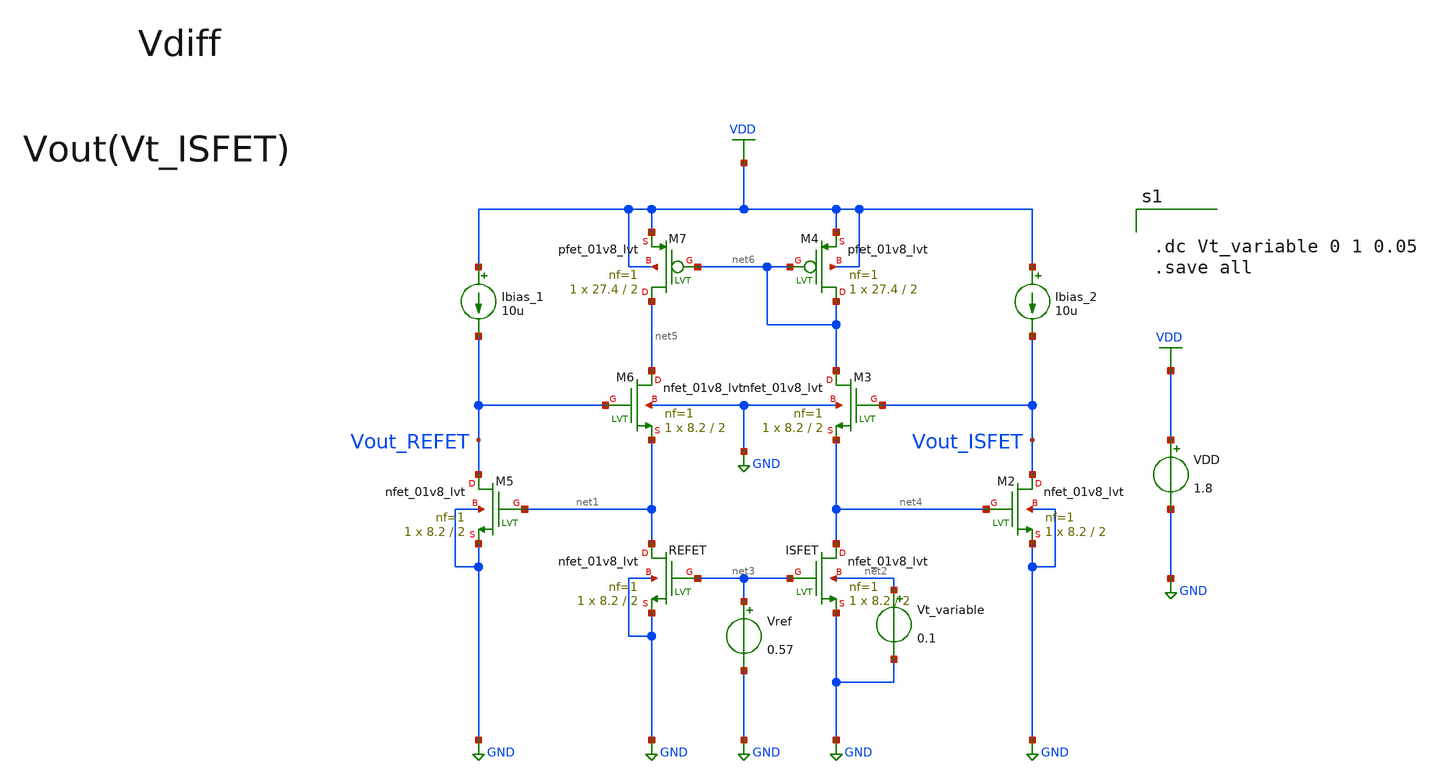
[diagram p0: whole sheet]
** sch_path: Voltage_Clamped_Configuration.sch
**.subckt Voltage_Clamped_Configuration
XISFET net4 net3 GND net2 sky130_fd_pr__nfet_01v8_lvt L=2 W=8.2 nf=1 ad='int((nf+1)/2) * W/nf * 0.29'
+ as='int((nf+2)/2) * W/nf * 0.29' pd='2*int((nf+1)/2) * (W/nf + 0.29)' ps='2*int((nf+2)/2) * (W/nf + 0.29)'
+ nrd='0.29 / W' nrs='0.29 / W' sa=0 sb=0 sd=0 mult=1 m=1
XM4 net6 net6 VDD VDD sky130_fd_pr__pfet_01v8_lvt L=2 W=27.4 nf=1 ad='int((nf+1)/2) * W/nf * 0.29' as='int((nf+2)/2) * W/nf * 0.29'
+ pd='2*int((nf+1)/2) * (W/nf + 0.29)' ps='2*int((nf+2)/2) * (W/nf + 0.29)' nrd='0.29 / W' nrs='0.29 / W'
+ sa=0 sb=0 sd=0 mult=1 m=1
XREFET net1 net3 GND GND sky130_fd_pr__nfet_01v8_lvt L=2 W=8.2 nf=1 ad='int((nf+1)/2) * W/nf * 0.29'
+ as='int((nf+2)/2) * W/nf * 0.29' pd='2*int((nf+1)/2) * (W/nf + 0.29)' ps='2*int((nf+2)/2) * (W/nf + 0.29)'
+ nrd='0.29 / W' nrs='0.29 / W' sa=0 sb=0 sd=0 mult=1 m=1
XM3 net6 Vout_ISFET net4 GND sky130_fd_pr__nfet_01v8_lvt L=2 W=8.2 nf=1 ad='int((nf+1)/2) * W/nf * 0.29'
+ as='int((nf+2)/2) * W/nf * 0.29' pd='2*int((nf+1)/2) * (W/nf + 0.29)' ps='2*int((nf+2)/2) * (W/nf + 0.29)'
+ nrd='0.29 / W' nrs='0.29 / W' sa=0 sb=0 sd=0 mult=1 m=1
XM6 net5 Vout_REFET net1 GND sky130_fd_pr__nfet_01v8_lvt L=2 W=8.2 nf=1 ad='int((nf+1)/2) * W/nf * 0.29'
+ as='int((nf+2)/2) * W/nf * 0.29' pd='2*int((nf+1)/2) * (W/nf + 0.29)' ps='2*int((nf+2)/2) * (W/nf + 0.29)'
+ nrd='0.29 / W' nrs='0.29 / W' sa=0 sb=0 sd=0 mult=1 m=1
XM7 net5 net6 VDD VDD sky130_fd_pr__pfet_01v8_lvt L=2 W=27.4 nf=1 ad='int((nf+1)/2) * W/nf * 0.29' as='int((nf+2)/2) * W/nf * 0.29'
+ pd='2*int((nf+1)/2) * (W/nf + 0.29)' ps='2*int((nf+2)/2) * (W/nf + 0.29)' nrd='0.29 / W' nrs='0.29 / W'
+ sa=0 sb=0 sd=0 mult=1 m=1
XM2 Vout_ISFET net4 GND GND sky130_fd_pr__nfet_01v8_lvt L=2 W=8.2 nf=1 ad='int((nf+1)/2) * W/nf * 0.29'
+ as='int((nf+2)/2) * W/nf * 0.29' pd='2*int((nf+1)/2) * (W/nf + 0.29)' ps='2*int((nf+2)/2) * (W/nf + 0.29)'
+ nrd='0.29 / W' nrs='0.29 / W' sa=0 sb=0 sd=0 mult=1 m=1
XM5 Vout_REFET net1 GND GND sky130_fd_pr__nfet_01v8_lvt L=2 W=8.2 nf=1 ad='int((nf+1)/2) * W/nf * 0.29'
+ as='int((nf+2)/2) * W/nf * 0.29' pd='2*int((nf+1)/2) * (W/nf + 0.29)' ps='2*int((nf+2)/2) * (W/nf + 0.29)'
+ nrd='0.29 / W' nrs='0.29 / W' sa=0 sb=0 sd=0 mult=1 m=1
VDD VDD GND 1.8
Ibias_2 VDD Vout_ISFET 10u
Ibias_1 VDD Vout_REFET 10u
Vref net3 GND 0.57
Vt_variable net2 GND 0.1
**** begin user architecture code

** opencircuitdesign pdks install
.lib $::SKYWATER_MODELS/sky130.lib.spice tt



.dc Vt_variable 0 1 0.05
.save all

**** end user architecture code
**.ends
.GLOBAL GND
.GLOBAL VDD
.end
